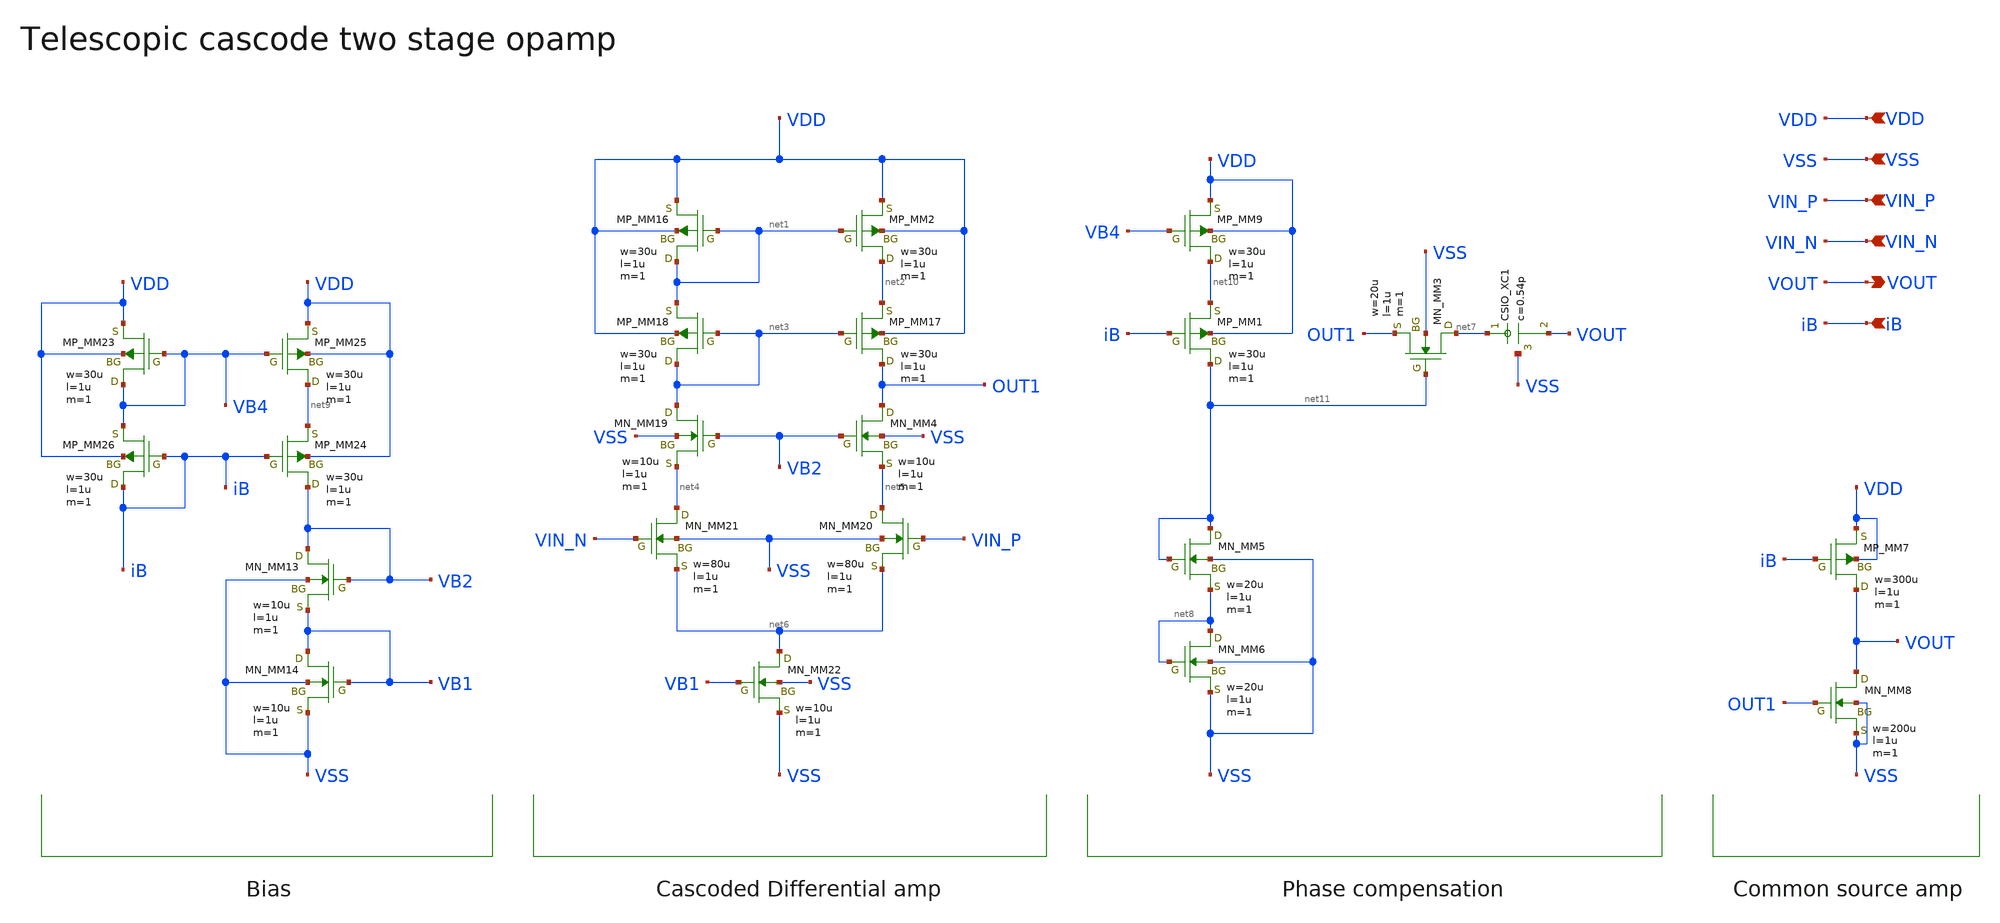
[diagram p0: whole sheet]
** sch_path: member_project/AM_Radio/Yamada3/xschem/cascode_opamp_2.sch
**.subckt cascode_opamp_2 VOUT VIN_N VIN_P VSS VDD iB
*.opin VOUT
*.ipin VIN_N
*.ipin VIN_P
*.ipin VSS
*.ipin VDD
*.ipin iB
MM2 net2 net1 VDD VDD PMOS w=30u l=1u as=0 ad=0 ps=0 pd=0 nrd=0 nrs=0 m=1
MM4 OUT1 VB2 net5 VSS NMOS w=10u l=1u as=0 ad=0 ps=0 pd=0 nrd=0 nrs=0 m=1
MM7 VOUT iB VDD VDD PMOS w=300u l=1u as=0 ad=0 ps=0 pd=0 nrd=0 nrs=0 m=1
MM8 VOUT OUT1 VSS VSS NMOS w=200u l=1u as=0 ad=0 ps=0 pd=0 nrd=0 nrs=0 m=1
MM16 net1 net1 VDD VDD PMOS w=30u l=1u as=0 ad=0 ps=0 pd=0 nrd=0 nrs=0 m=1
MM17 OUT1 net3 net2 VDD PMOS w=30u l=1u as=0 ad=0 ps=0 pd=0 nrd=0 nrs=0 m=1
MM18 net3 net3 net1 VDD PMOS w=30u l=1u as=0 ad=0 ps=0 pd=0 nrd=0 nrs=0 m=1
MM19 net3 VB2 net4 VSS NMOS w=10u l=1u as=0 ad=0 ps=0 pd=0 nrd=0 nrs=0 m=1
MM20 net5 VIN_P net6 VSS NMOS w=80u l=1u as=0 ad=0 ps=0 pd=0 nrd=0 nrs=0 m=1
MM21 net4 VIN_N net6 VSS NMOS w=80u l=1u as=0 ad=0 ps=0 pd=0 nrd=0 nrs=0 m=1
MM22 net6 VB1 VSS VSS NMOS w=10u l=1u as=0 ad=0 ps=0 pd=0 nrd=0 nrs=0 m=1
MM3 net7 net11 OUT1 VSS NMOS w=20u l=1u as=0 ad=0 ps=0 pd=0 nrd=0 nrs=0 m=1
MM6 net8 net8 VSS VSS NMOS w=20u l=1u as=0 ad=0 ps=0 pd=0 nrd=0 nrs=0 m=1
MM13 VB2 VB2 VB1 VSS NMOS w=10u l=1u as=0 ad=0 ps=0 pd=0 nrd=0 nrs=0 m=1
MM14 VB1 VB1 VSS VSS NMOS w=10u l=1u as=0 ad=0 ps=0 pd=0 nrd=0 nrs=0 m=1
MM23 VB4 VB4 VDD VDD PMOS w=30u l=1u as=0 ad=0 ps=0 pd=0 nrd=0 nrs=0 m=1
MM24 VB2 iB net9 VDD PMOS w=30u l=1u as=0 ad=0 ps=0 pd=0 nrd=0 nrs=0 m=1
MM25 net9 VB4 VDD VDD PMOS w=30u l=1u as=0 ad=0 ps=0 pd=0 nrd=0 nrs=0 m=1
MM26 iB iB VB4 VDD PMOS w=30u l=1u as=0 ad=0 ps=0 pd=0 nrd=0 nrs=0 m=1
MM1 net11 iB net10 VDD PMOS w=30u l=1u as=0 ad=0 ps=0 pd=0 nrd=0 nrs=0 m=1
MM9 net10 VB4 VDD VDD PMOS w=30u l=1u as=0 ad=0 ps=0 pd=0 nrd=0 nrs=0 m=1
MM5 net11 net11 net8 VSS NMOS w=20u l=1u as=0 ad=0 ps=0 pd=0 nrd=0 nrs=0 m=1
XXC1 net7 VOUT VSS F_CSIO c=0.54p x=30u y=30u m=1
**.ends
.end
